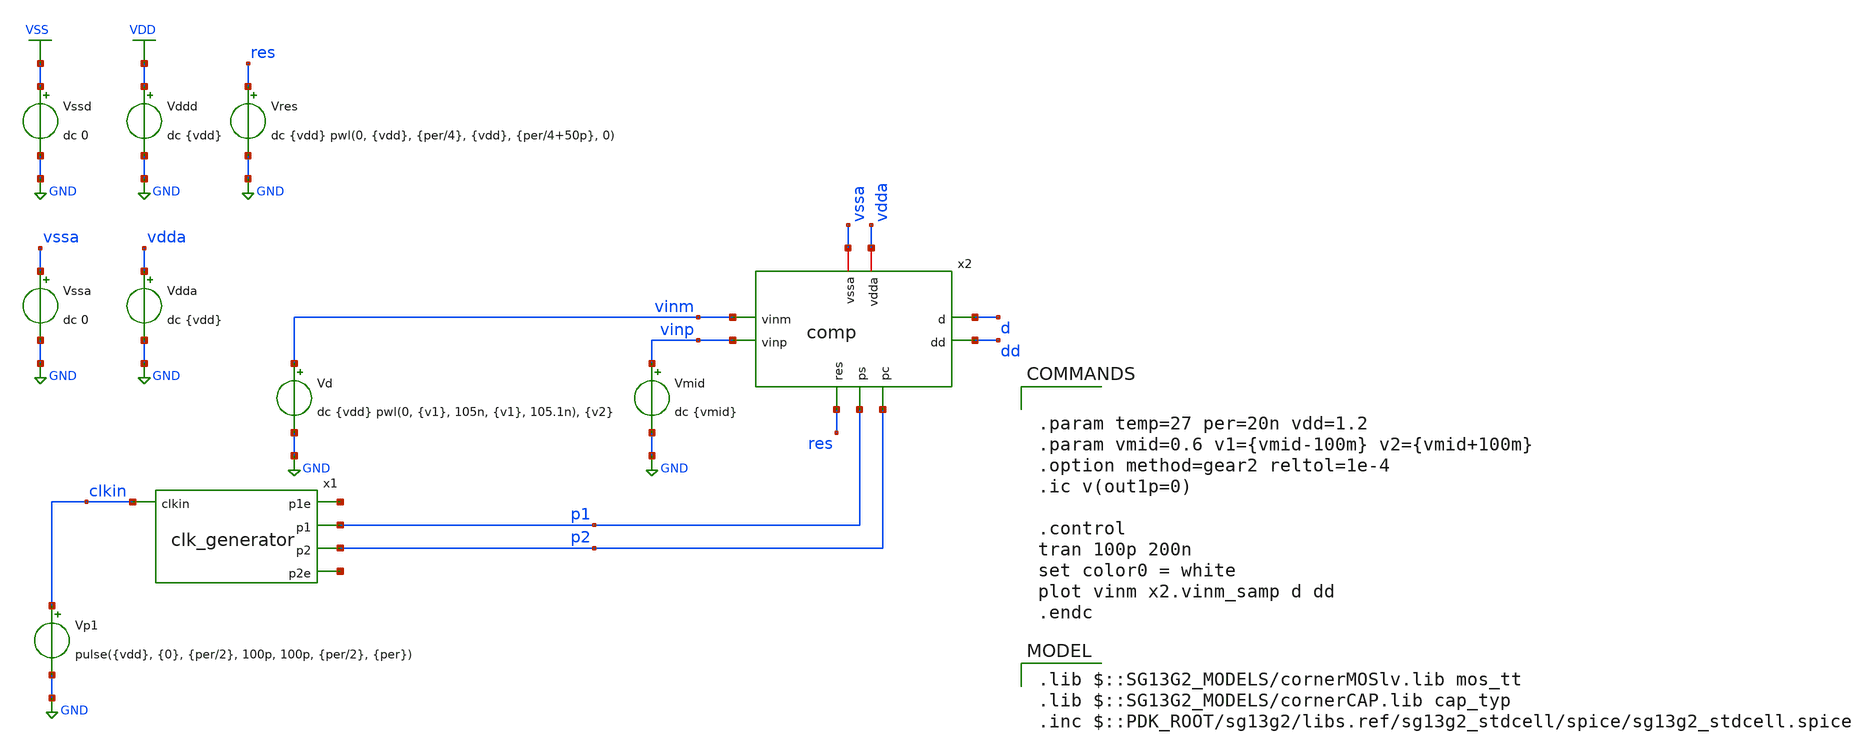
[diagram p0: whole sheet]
** sch_path: schematics/tb_comp.sch
**.subckt tb_comp
Vddd VDD GND dc {vdd}
Vssd VSS GND dc 0
Vp1 clkin GND pulse({vdd}, {0}, {per/2}, 100p, 100p, {per/2}, {per})
x1 net1 clkin p1 p2 net2 clk_generator
Vmid vinp GND dc {vmid}
Vres res GND dc {vdd} pwl(0, {vdd}, {per/4}, {vdd}, {per/4+50p}, 0)
Vssa vssa GND dc 0
Vdda vdda GND dc {vdd}
Vd vinm GND dc {vdd} pwl(0, {v1}, 105n, {v1}, 105.1n), {v2}
x2 p2 d dd vinp vssa p1 res vinm vdda comp
**** begin user architecture code


.param temp=27 per=20n vdd=1.2
.param vmid=0.6 v1={vmid-100m} v2={vmid+100m}
.option method=gear2 reltol=1e-4
.ic v(out1p=0)

.control
tran 100p 200n
set color0 = white
plot vinm x2.vinm_samp d dd
.endc


 .lib $::SG13G2_MODELS/cornerMOSlv.lib mos_tt
.lib $::SG13G2_MODELS/cornerCAP.lib cap_typ
.inc $::PDK_ROOT/sg13g2/libs.ref/sg13g2_stdcell/spice/sg13g2_stdcell.spice

**** end user architecture code
**.ends
.GLOBAL VDD
.GLOBAL GND
.GLOBAL VSS
.end
